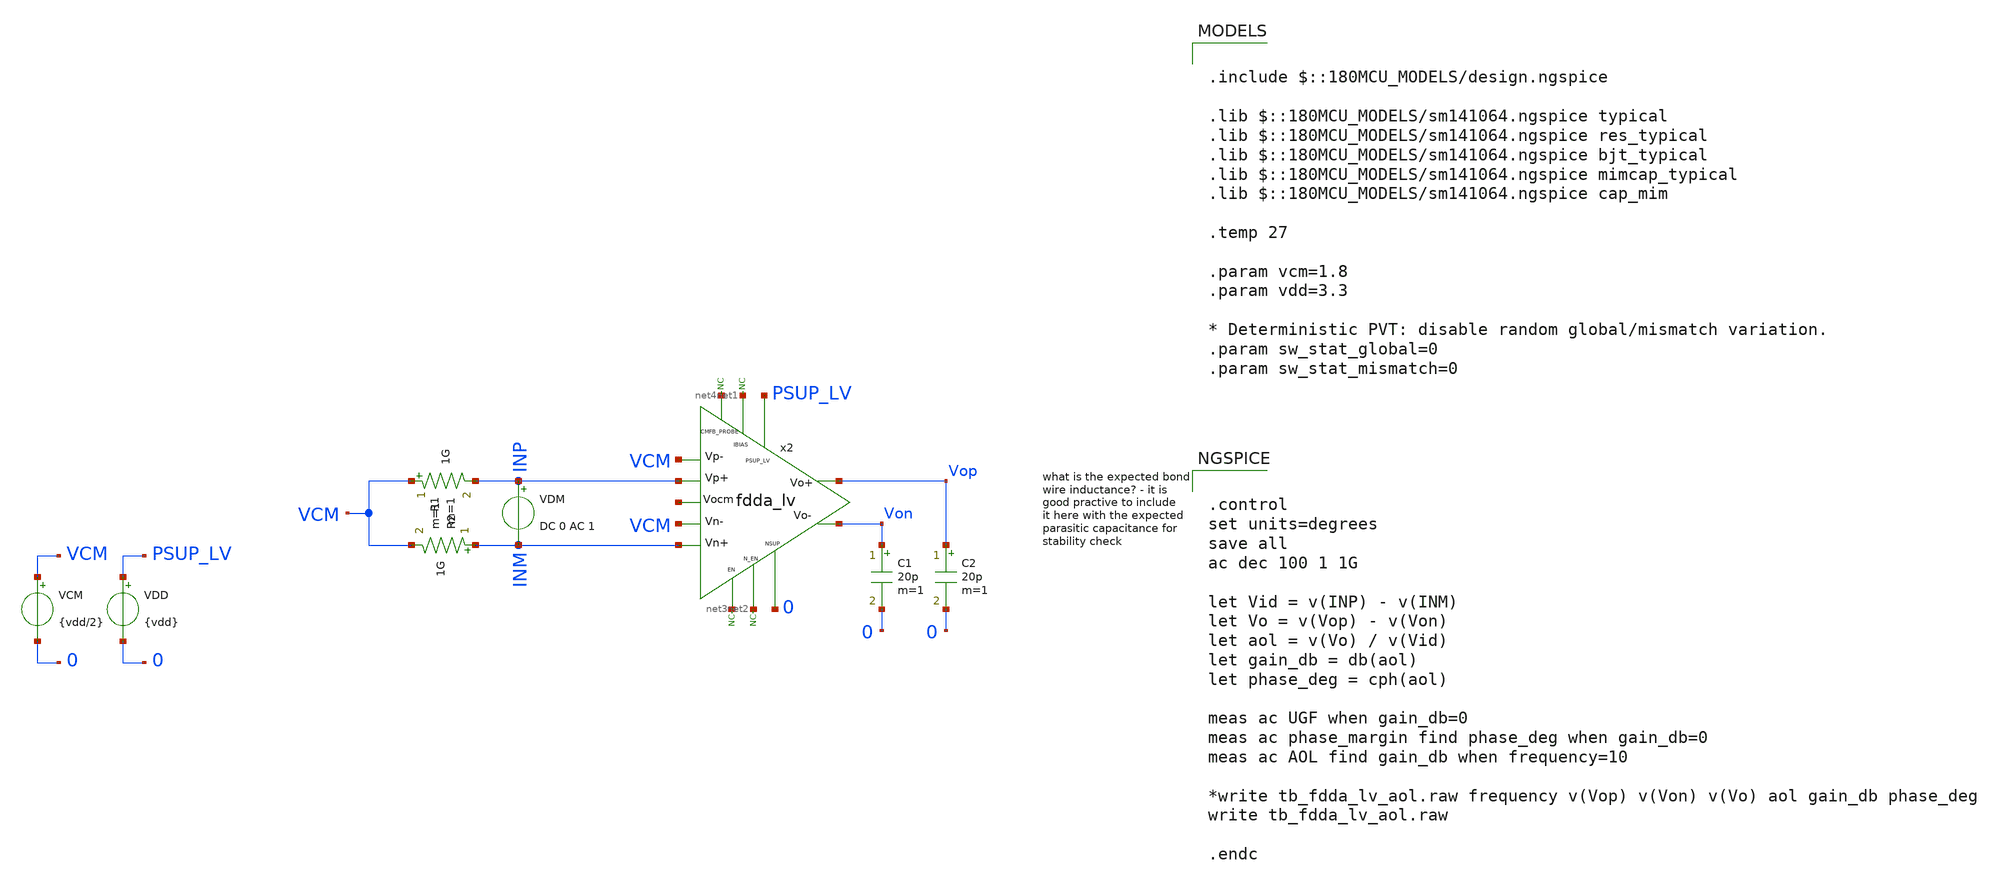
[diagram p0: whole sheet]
** sch_path: xschem/blocks/fdda_lv/tb_fdda_lv_aol.sch
**.subckt tb_fdda_lv_aol
C1 Von 0 20p m=1
x2 PSUP_LV VCM VCM INM INP Vop Von net1 net2 net3 0 net4 net5 fdda_lv
* noconn #net1
* noconn #net3
* noconn #net2
VDD PSUP_LV 0 {vdd}
C2 Vop 0 20p m=1
VCM VCM 0 {vdd/2}
* noconn #net4
VDM INP INM DC 0 AC 1
R1 VCM INP 1G m=1
R2 INM VCM 1G m=1
**** begin user architecture code

.include $::180MCU_MODELS/design.ngspice

.lib $::180MCU_MODELS/sm141064.ngspice typical
.lib $::180MCU_MODELS/sm141064.ngspice res_typical
.lib $::180MCU_MODELS/sm141064.ngspice bjt_typical
.lib $::180MCU_MODELS/sm141064.ngspice mimcap_typical
.lib $::180MCU_MODELS/sm141064.ngspice cap_mim

.temp 27

.param vcm=1.8
.param vdd=3.3

* Deterministic PVT: disable random global/mismatch variation.
.param sw_stat_global=0
.param sw_stat_mismatch=0



.control
set units=degrees
save all
ac dec 100 1 1G

let Vid = v(INP) - v(INM)
let Vo = v(Vop) - v(Von)
let aol = v(Vo) / v(Vid)
let gain_db = db(aol)
let phase_deg = cph(aol)

meas ac UGF when gain_db=0
meas ac phase_margin find phase_deg when gain_db=0
meas ac AOL find gain_db when frequency=10

*write tb_fdda_lv_aol.raw frequency v(Vop) v(Von) v(Vo) aol gain_db phase_deg
write tb_fdda_lv_aol.raw

.endc


**** end user architecture code
**.ends
.end
